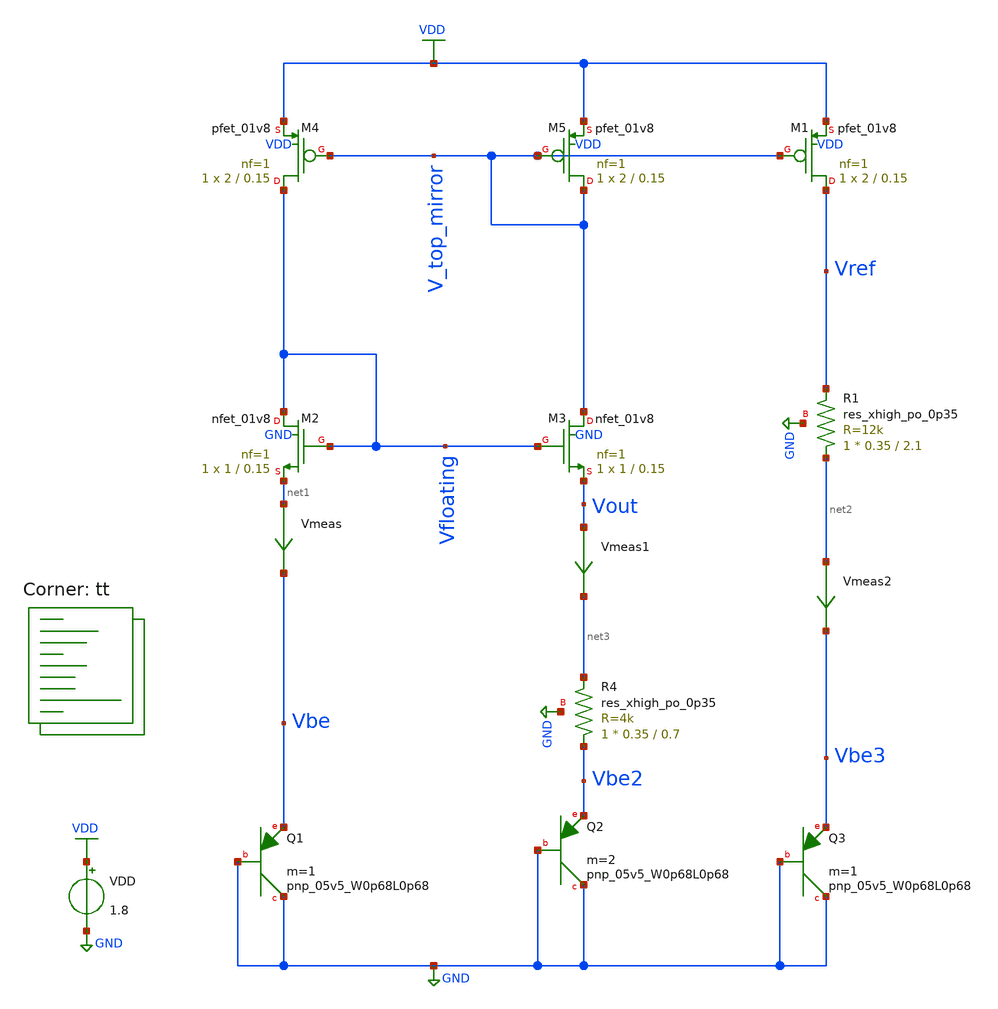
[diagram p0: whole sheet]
** sch_path: projects/bandgapref/xschem_ngspice/old_files/mos_bandgap5.sch
**.subckt mos_bandgap5
XM2 Vfloating Vfloating net1 GND sky130_fd_pr__nfet_01v8 L=0.15 W=1 nf=1 ad='int((nf+1)/2) * W/nf * 0.29'
+ as='int((nf+2)/2) * W/nf * 0.29' pd='2*int((nf+1)/2) * (W/nf + 0.29)' ps='2*int((nf+2)/2) * (W/nf + 0.29)'
+ nrd='0.29 / W' nrs='0.29 / W' sa=0 sb=0 sd=0 mult=1 m=1
XM3 V_top_mirror Vfloating Vout GND sky130_fd_pr__nfet_01v8 L=0.15 W=1 nf=1 ad='int((nf+1)/2) * W/nf * 0.29'
+ as='int((nf+2)/2) * W/nf * 0.29' pd='2*int((nf+1)/2) * (W/nf + 0.29)' ps='2*int((nf+2)/2) * (W/nf + 0.29)'
+ nrd='0.29 / W' nrs='0.29 / W' sa=0 sb=0 sd=0 mult=1 m=1
XM4 Vfloating V_top_mirror VDD VDD sky130_fd_pr__pfet_01v8 L=0.15 W=2 nf=1 ad='int((nf+1)/2) * W/nf * 0.29'
+ as='int((nf+2)/2) * W/nf * 0.29' pd='2*int((nf+1)/2) * (W/nf + 0.29)' ps='2*int((nf+2)/2) * (W/nf + 0.29)'
+ nrd='0.29 / W' nrs='0.29 / W' sa=0 sb=0 sd=0 mult=1 m=1
XM5 V_top_mirror V_top_mirror VDD VDD sky130_fd_pr__pfet_01v8 L=0.15 W=2 nf=1 ad='int((nf+1)/2) * W/nf * 0.29'
+ as='int((nf+2)/2) * W/nf * 0.29' pd='2*int((nf+1)/2) * (W/nf + 0.29)' ps='2*int((nf+2)/2) * (W/nf + 0.29)'
+ nrd='0.29 / W' nrs='0.29 / W' sa=0 sb=0 sd=0 mult=1 m=1
VDD VDD GND 1.8
Vmeas net1 Vbe 0
.save i(vmeas)
Vmeas1 Vout net3 0
.save i(vmeas1)
Vmeas2 net2 Vbe3 0
.save i(vmeas2)
XM1 Vref V_top_mirror VDD VDD sky130_fd_pr__pfet_01v8 L=0.15 W=2 nf=1 ad='int((nf+1)/2) * W/nf * 0.29'
+ as='int((nf+2)/2) * W/nf * 0.29' pd='2*int((nf+1)/2) * (W/nf + 0.29)' ps='2*int((nf+2)/2) * (W/nf + 0.29)'
+ nrd='0.29 / W' nrs='0.29 / W' sa=0 sb=0 sd=0 mult=1 m=1
XR4 Vbe2 net3 GND sky130_fd_pr__res_xhigh_po_0p35 L=0.7 mult=1 m=1
XR1 net2 Vref GND sky130_fd_pr__res_xhigh_po_0p35 L=2.1 mult=1 m=1
XQ1 GND GND Vbe sky130_fd_pr__pnp_05v5_W0p68L0p68 m=1
XQ2 GND GND Vbe2 sky130_fd_pr__pnp_05v5_W0p68L0p68 m=2
XQ3 GND GND Vbe3 sky130_fd_pr__pnp_05v5_W0p68L0p68 m=1
**** begin user architecture code
.lib $::SKYWATER_MODELS/sky130.lib.spice tt



.option method=gear
.option wnflag=1
.option savecurrents

.param VDDGAUSS = agauss(3.3, 0.05, 1)
.param VDD = VDDGAUSS
** use following line to remove VCC variations
* .param VDD = 3.3

.save @m.xm1.sky130_fd_pr__nfet_01v8 [gm] @m.xm2.sky130_fd_pr__nfet_01v8 [gm] @m.xm3.sky130_fd_pr__nfet_01v8 [gm] @m.xm4.sky130_fd_pr__nfet_01v8 [gm] @m.xm5.sky130_fd_pr__nfet_01v8 [gm]


.control
*  option seed=9
*  let run=0
*  dowhile run <= 10
save all
op
*tran 10ns 500us
dc VDD 0 3.3 0.1
* dc temp -40 120 2 VDD 1.8 3.3 0.2
remzerovec
write mos_bandgap5.raw
set appendwrite
*    reset
*    let run = run + 1
*  end
.endc



**** end user architecture code
**.ends
.GLOBAL GND
.GLOBAL VDD
.end
